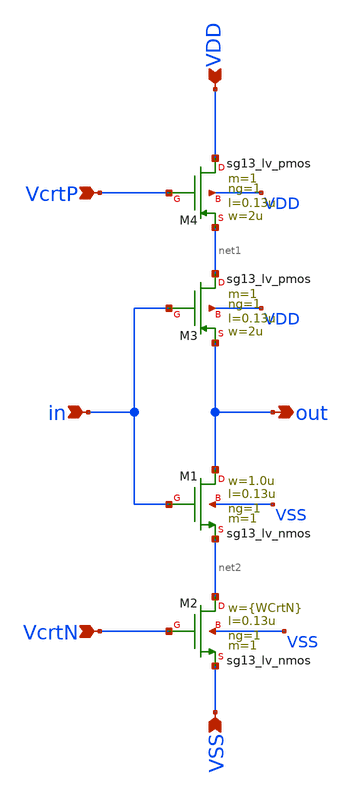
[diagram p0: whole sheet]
** sch_path: work/gate_cs_inv/xschem/cs_inv.sch
**.subckt cs_inv VDD VSS in out VcrtP VcrtN
*.ipin VDD
*.ipin VSS
*.ipin in
*.opin out
*.ipin VcrtP
*.ipin VcrtN
XM1 out in net2 VSS sg13_lv_nmos w=1.0u l=0.13u ng=1 m=1 mm_ok=1
XM2 net2 VcrtN VSS VSS sg13_lv_nmos w={WCrtN} l=0.13u ng=1 m=1 mm_ok=1
XM3 net1 in out VDD sg13_lv_pmos w=2u l=0.13u ng=1 m=1 mm_ok=1
XM4 VDD VcrtP net1 VDD sg13_lv_pmos w=2u l=0.13u ng=1 m=1 mm_ok=1
**.ends
.end
